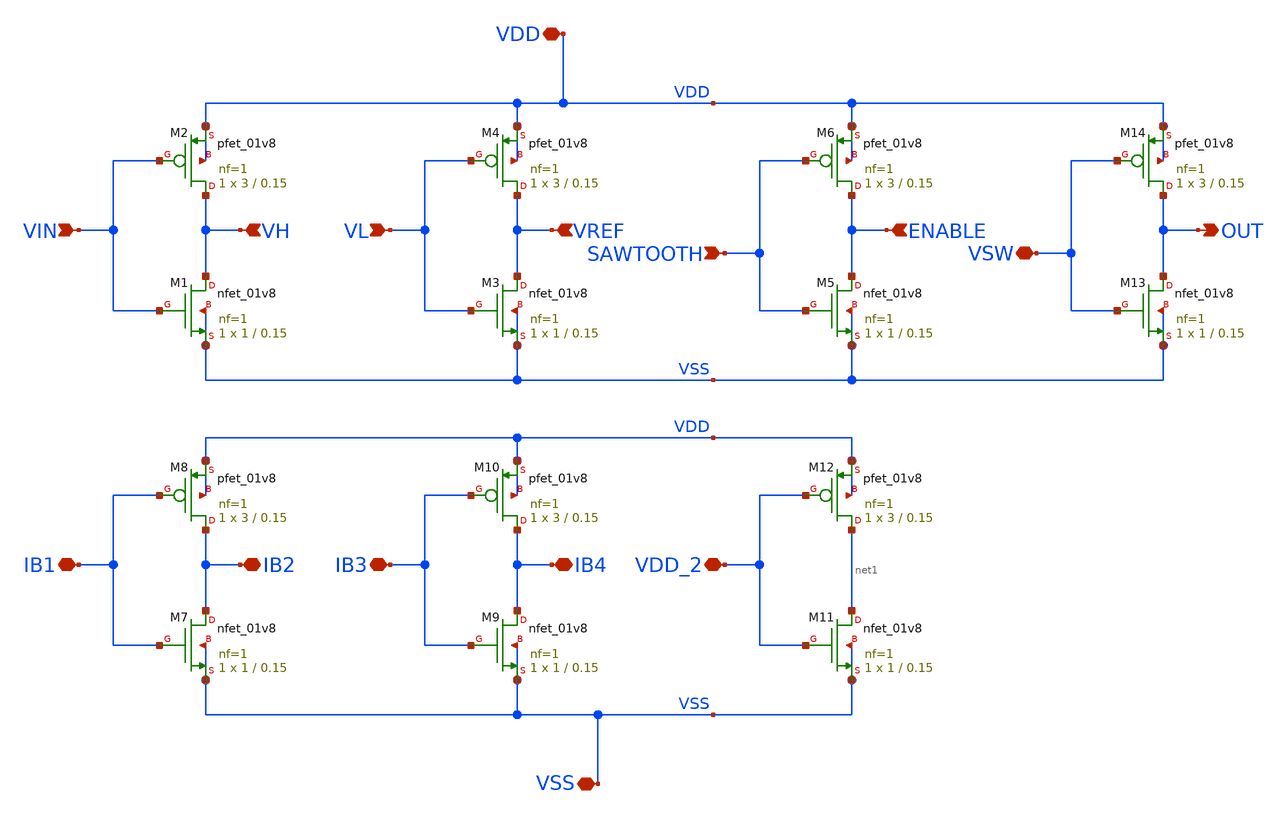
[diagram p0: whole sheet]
** sch_path: xschem/DC_DC_Converter_xschem/OTHERS/Pre_Checks/Dummy_ckt.sch
**.subckt Dummy_ckt VIN VDD VSS VH VL VREF SAWTOOTH ENABLE IB1 VSW OUT IB2 IB3 IB4 VDD_2
*.ipin VIN
*.iopin VDD
*.iopin VSS
*.ipin VH
*.ipin VL
*.ipin VREF
*.ipin SAWTOOTH
*.ipin ENABLE
*.iopin IB1
*.iopin VSW
*.opin OUT
*.iopin IB2
*.iopin IB3
*.iopin IB4
*.iopin VDD_2
XM1 VH VIN VSS VSS sky130_fd_pr__nfet_01v8 L=0.15 W=1 nf=1 ad='int((nf+1)/2) * W/nf * 0.29' as='int((nf+2)/2) * W/nf * 0.29'
+ pd='2*int((nf+1)/2) * (W/nf + 0.29)' ps='2*int((nf+2)/2) * (W/nf + 0.29)' nrd='0.29 / W' nrs='0.29 / W'
+ sa=0 sb=0 sd=0 mult=1 m=1
XM2 VH VIN VDD VDD sky130_fd_pr__pfet_01v8 L=0.15 W=3 nf=1 ad='int((nf+1)/2) * W/nf * 0.29' as='int((nf+2)/2) * W/nf * 0.29'
+ pd='2*int((nf+1)/2) * (W/nf + 0.29)' ps='2*int((nf+2)/2) * (W/nf + 0.29)' nrd='0.29 / W' nrs='0.29 / W'
+ sa=0 sb=0 sd=0 mult=1 m=1
XM3 VREF VL VSS VSS sky130_fd_pr__nfet_01v8 L=0.15 W=1 nf=1 ad='int((nf+1)/2) * W/nf * 0.29' as='int((nf+2)/2) * W/nf * 0.29'
+ pd='2*int((nf+1)/2) * (W/nf + 0.29)' ps='2*int((nf+2)/2) * (W/nf + 0.29)' nrd='0.29 / W' nrs='0.29 / W'
+ sa=0 sb=0 sd=0 mult=1 m=1
XM4 VREF VL VDD VDD sky130_fd_pr__pfet_01v8 L=0.15 W=3 nf=1 ad='int((nf+1)/2) * W/nf * 0.29' as='int((nf+2)/2) * W/nf * 0.29'
+ pd='2*int((nf+1)/2) * (W/nf + 0.29)' ps='2*int((nf+2)/2) * (W/nf + 0.29)' nrd='0.29 / W' nrs='0.29 / W'
+ sa=0 sb=0 sd=0 mult=1 m=1
XM5 ENABLE SAWTOOTH VSS VSS sky130_fd_pr__nfet_01v8 L=0.15 W=1 nf=1 ad='int((nf+1)/2) * W/nf * 0.29'
+ as='int((nf+2)/2) * W/nf * 0.29' pd='2*int((nf+1)/2) * (W/nf + 0.29)' ps='2*int((nf+2)/2) * (W/nf + 0.29)'
+ nrd='0.29 / W' nrs='0.29 / W' sa=0 sb=0 sd=0 mult=1 m=1
XM6 ENABLE SAWTOOTH VDD VDD sky130_fd_pr__pfet_01v8 L=0.15 W=3 nf=1 ad='int((nf+1)/2) * W/nf * 0.29'
+ as='int((nf+2)/2) * W/nf * 0.29' pd='2*int((nf+1)/2) * (W/nf + 0.29)' ps='2*int((nf+2)/2) * (W/nf + 0.29)'
+ nrd='0.29 / W' nrs='0.29 / W' sa=0 sb=0 sd=0 mult=1 m=1
XM7 IB2 IB1 VSS VSS sky130_fd_pr__nfet_01v8 L=0.15 W=1 nf=1 ad='int((nf+1)/2) * W/nf * 0.29' as='int((nf+2)/2) * W/nf * 0.29'
+ pd='2*int((nf+1)/2) * (W/nf + 0.29)' ps='2*int((nf+2)/2) * (W/nf + 0.29)' nrd='0.29 / W' nrs='0.29 / W'
+ sa=0 sb=0 sd=0 mult=1 m=1
XM8 IB2 IB1 VDD VDD sky130_fd_pr__pfet_01v8 L=0.15 W=3 nf=1 ad='int((nf+1)/2) * W/nf * 0.29' as='int((nf+2)/2) * W/nf * 0.29'
+ pd='2*int((nf+1)/2) * (W/nf + 0.29)' ps='2*int((nf+2)/2) * (W/nf + 0.29)' nrd='0.29 / W' nrs='0.29 / W'
+ sa=0 sb=0 sd=0 mult=1 m=1
XM9 IB4 IB3 VSS VSS sky130_fd_pr__nfet_01v8 L=0.15 W=1 nf=1 ad='int((nf+1)/2) * W/nf * 0.29' as='int((nf+2)/2) * W/nf * 0.29'
+ pd='2*int((nf+1)/2) * (W/nf + 0.29)' ps='2*int((nf+2)/2) * (W/nf + 0.29)' nrd='0.29 / W' nrs='0.29 / W'
+ sa=0 sb=0 sd=0 mult=1 m=1
XM10 IB4 IB3 VDD VDD sky130_fd_pr__pfet_01v8 L=0.15 W=3 nf=1 ad='int((nf+1)/2) * W/nf * 0.29' as='int((nf+2)/2) * W/nf * 0.29'
+ pd='2*int((nf+1)/2) * (W/nf + 0.29)' ps='2*int((nf+2)/2) * (W/nf + 0.29)' nrd='0.29 / W' nrs='0.29 / W'
+ sa=0 sb=0 sd=0 mult=1 m=1
XM11 net1 VDD_2 VSS VSS sky130_fd_pr__nfet_01v8 L=0.15 W=1 nf=1 ad='int((nf+1)/2) * W/nf * 0.29' as='int((nf+2)/2) * W/nf * 0.29'
+ pd='2*int((nf+1)/2) * (W/nf + 0.29)' ps='2*int((nf+2)/2) * (W/nf + 0.29)' nrd='0.29 / W' nrs='0.29 / W'
+ sa=0 sb=0 sd=0 mult=1 m=1
XM12 net1 VDD_2 VDD VDD sky130_fd_pr__pfet_01v8 L=0.15 W=3 nf=1 ad='int((nf+1)/2) * W/nf * 0.29' as='int((nf+2)/2) * W/nf * 0.29'
+ pd='2*int((nf+1)/2) * (W/nf + 0.29)' ps='2*int((nf+2)/2) * (W/nf + 0.29)' nrd='0.29 / W' nrs='0.29 / W'
+ sa=0 sb=0 sd=0 mult=1 m=1
XM13 OUT VSW VSS VSS sky130_fd_pr__nfet_01v8 L=0.15 W=1 nf=1 ad='int((nf+1)/2) * W/nf * 0.29' as='int((nf+2)/2) * W/nf * 0.29'
+ pd='2*int((nf+1)/2) * (W/nf + 0.29)' ps='2*int((nf+2)/2) * (W/nf + 0.29)' nrd='0.29 / W' nrs='0.29 / W'
+ sa=0 sb=0 sd=0 mult=1 m=1
XM14 OUT VSW VDD VDD sky130_fd_pr__pfet_01v8 L=0.15 W=3 nf=1 ad='int((nf+1)/2) * W/nf * 0.29' as='int((nf+2)/2) * W/nf * 0.29'
+ pd='2*int((nf+1)/2) * (W/nf + 0.29)' ps='2*int((nf+2)/2) * (W/nf + 0.29)' nrd='0.29 / W' nrs='0.29 / W'
+ sa=0 sb=0 sd=0 mult=1 m=1
**.ends
.end
